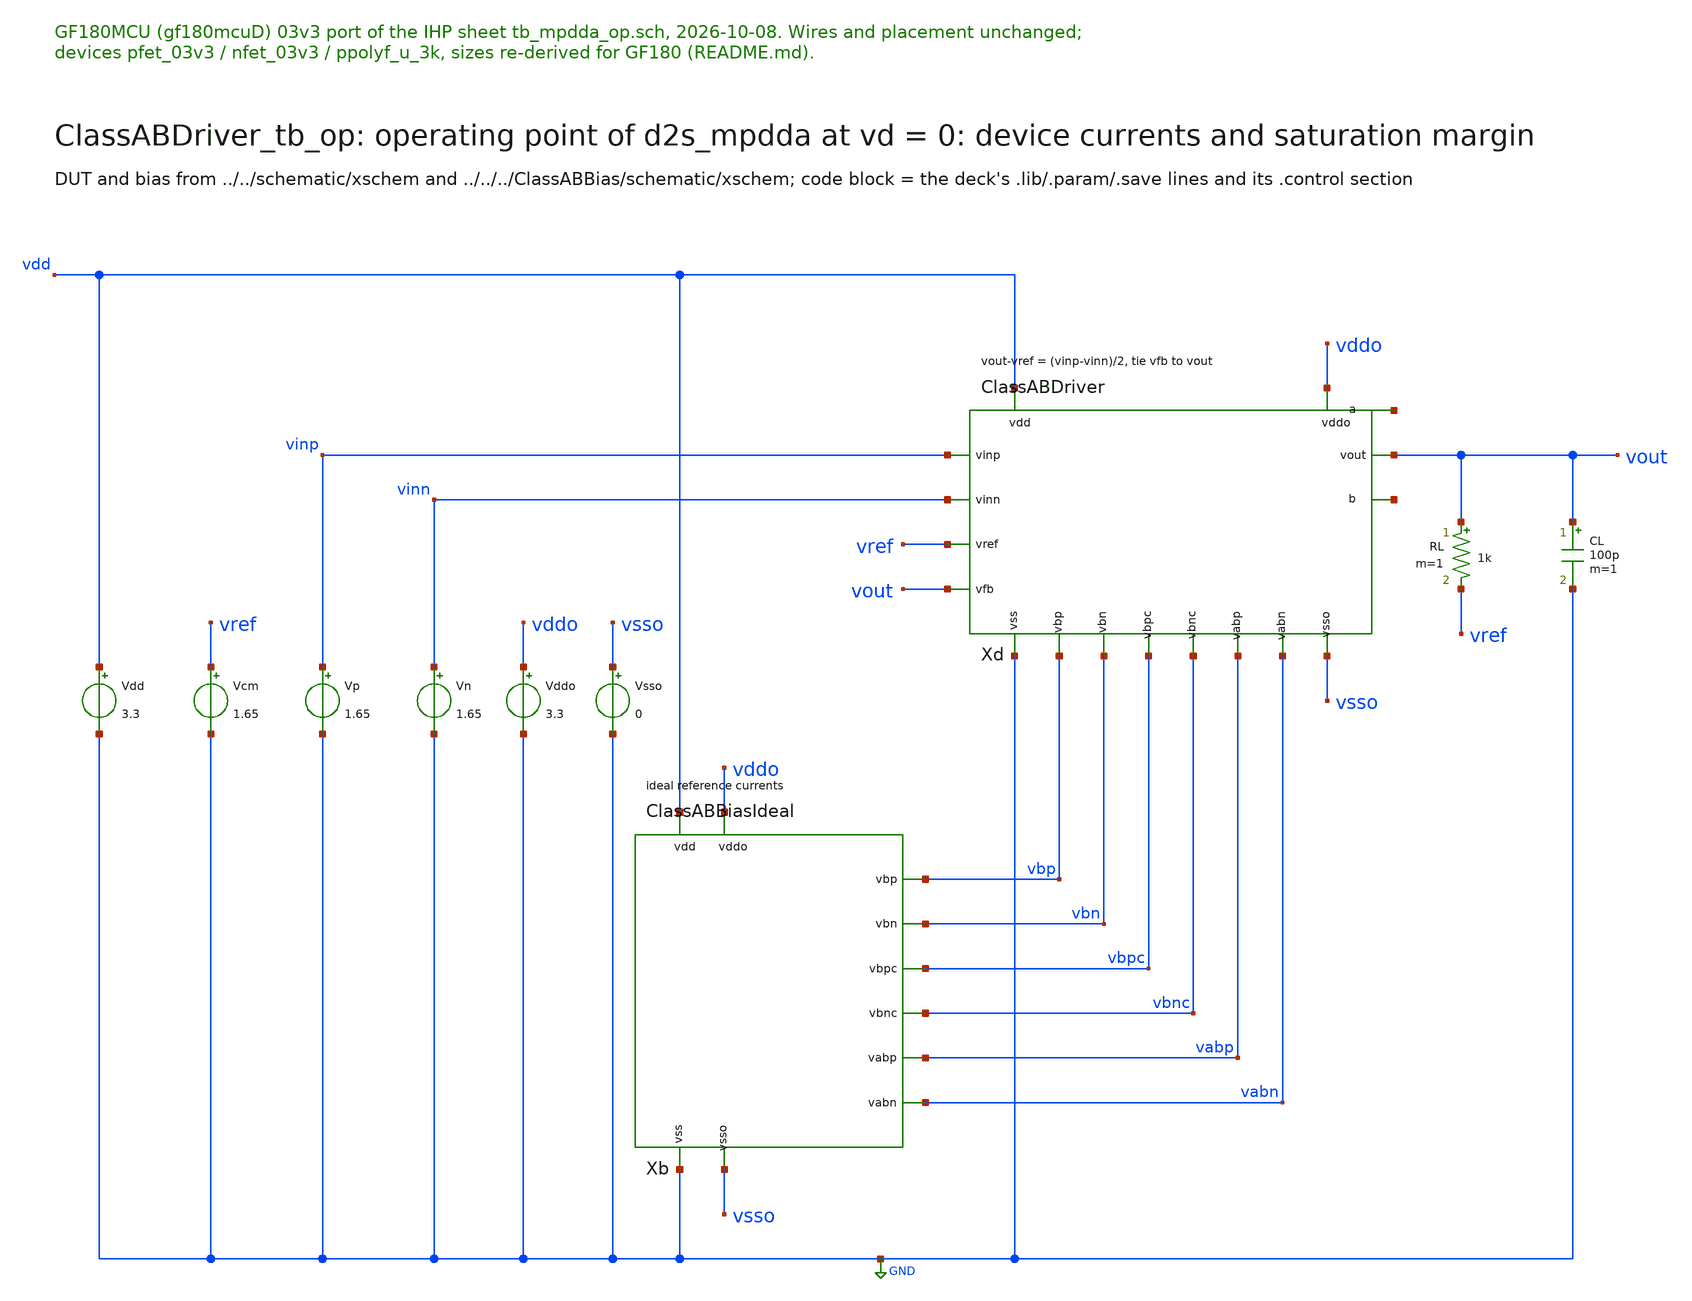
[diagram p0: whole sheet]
** sch_path: macros/ClassABDriver/testbenches/xschem/ClassABDriver_tb_op.sch
**.subckt ClassABDriver_tb_op
Vdd vdd GND 3.3
Vcm vref GND 1.65
Xb vdd GND vddo vsso vbp vbn vbpc vbnc vabp vabn ClassABBiasIdeal
Xd vdd GND vddo vsso vinp vinn vref vout vout vbp vbn vbpc vbnc vabp vabn net1 net2 ClassABDriver
Vp vinp GND 1.65
Vn vinn GND 1.65
RL vout vref 1k m=1
CL vout GND 100p m=1
Vddo vddo GND 3.3
Vsso vsso GND 0
**** begin user architecture code

.control
op
print v(xd.x) v(xd.y) v(xd.a) v(xd.b) v(xd.l1) v(xd.l2) v(xd.pl) v(xd.pr) i(vdd) i(vddo)
print @m.xd.xsx.m0[id] @m.xd.xsx.m0[vds] @m.xd.xsx.m0[vdsat]
print @m.xd.xsy.m0[id] @m.xd.xsy.m0[vds] @m.xd.xsy.m0[vdsat]
print @m.xd.xcx.m0[id] @m.xd.xcx.m0[vds] @m.xd.xcx.m0[vdsat]
print @m.xd.xcy.m0[id] @m.xd.xcy.m0[vds] @m.xd.xcy.m0[vdsat]
print @m.xd.xfnl.m0[id] @m.xd.xfnl.m0[vds] @m.xd.xfnl.m0[vdsat]
print @m.xd.xabn.m0[id] @m.xd.xabn.m0[vds] @m.xd.xabn.m0[vdsat]
print @m.xd.xon.m0[id] @m.xd.xon.m0[vds] @m.xd.xon.m0[vdsat]
print @m.xd.xpl.m0[id] @m.xd.xpl.m0[vds] @m.xd.xpl.m0[vdsat]
print @m.xd.xpr.m0[id] @m.xd.xpr.m0[vds] @m.xd.xpr.m0[vdsat]
print @m.xd.xpcl.m0[id] @m.xd.xpcl.m0[vds] @m.xd.xpcl.m0[vdsat]
print @m.xd.xpcr.m0[id] @m.xd.xpcr.m0[vds] @m.xd.xpcr.m0[vdsat]
print @m.xd.xfpl.m0[id] @m.xd.xfpl.m0[vds] @m.xd.xfpl.m0[vdsat]
print @m.xd.xabp.m0[id] @m.xd.xabp.m0[vds] @m.xd.xabp.m0[vdsat]
print @m.xd.xop.m0[id] @m.xd.xop.m0[vds] @m.xd.xop.m0[vdsat]
.endc


.include $::180MCU_MODELS/design.ngspice
.lib $::180MCU_MODELS/sm141064.ngspice typical
.lib $::180MCU_MODELS/sm141064.ngspice res_typical
.lib $::180MCU_MODELS/sm141064.ngspice moscap_typical

**** end user architecture code
**.ends
.GLOBAL GND
.end
